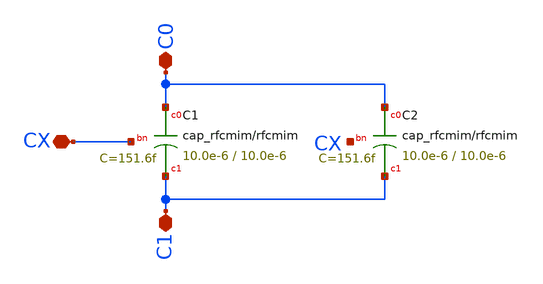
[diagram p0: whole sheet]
** sch_path: multiplier_support/schematic/sg13_rf_cmim_2x.sch
**.subckt sg13_rf_cmim_2x C0 C1 CX
*.iopin C0
*.iopin C1
*.iopin CX
XC1 C0 C1 CX cap_rfcmim w=10.0e-6 l=10.0e-6 wfeed=5.0e-6 m=1 mm_ok=1
XC2 C0 C1 CX cap_rfcmim w=10.0e-6 l=10.0e-6 wfeed=5.0e-6 m=1 mm_ok=1
**.ends
.end
